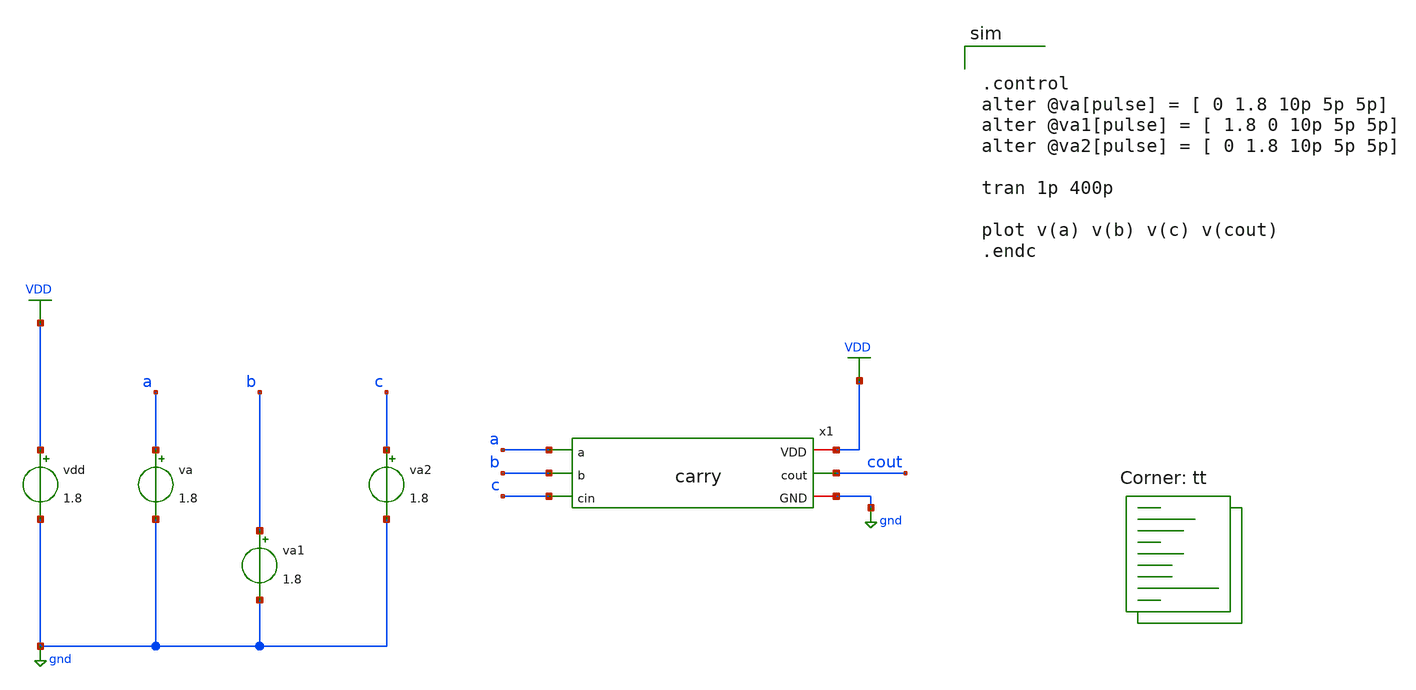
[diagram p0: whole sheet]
** sch_path: assignments/assignment7/carry_tb.sch
**.subckt carry_tb
x1 VDD a b c cout gnd carry
vdd VDD gnd 1.8
va a gnd 1.8
va1 b gnd 1.8
va2 c gnd 1.8
**** begin user architecture code


.control
alter @va[pulse] = [ 0 1.8 10p 5p 5p]
alter @va1[pulse] = [ 1.8 0 10p 5p 5p]
alter @va2[pulse] = [ 0 1.8 10p 5p 5p]

tran 1p 400p

plot v(a) v(b) v(c) v(cout)
.endc


.lib $::SKYWATER_MODELS/sky130.lib.spice tt
**** end user architecture code
**.ends

* expanding   symbol:  carry.sym # of pins=6
** sym_path: assignments/assignment7/carry.sym
** sch_path: assignments/assignment7/carry.sch
.subckt carry VDD a b cin cout GND
*.opin cout
*.ipin a
*.iopin VDD
*.iopin GND
*.ipin b
*.ipin cin
XM1 cout cin net3 GND sky130_fd_pr__nfet_01v8 L=0.15 W=0.84 nf=1 ad='int((nf+1)/2) * W/nf * 0.29' as='int((nf+2)/2) * W/nf * 0.29'
+ pd='2*int((nf+1)/2) * (W/nf + 0.29)' ps='2*int((nf+2)/2) * (W/nf + 0.29)' nrd='0.29 / W' nrs='0.29 / W'
+ sa=0 sb=0 sd=0 mult=1 m=1
XM2 net1 b VDD VDD sky130_fd_pr__pfet_01v8 L=0.15 W=1.68 nf=1 ad='int((nf+1)/2) * W/nf * 0.29' as='int((nf+2)/2) * W/nf * 0.29'
+ pd='2*int((nf+1)/2) * (W/nf + 0.29)' ps='2*int((nf+2)/2) * (W/nf + 0.29)' nrd='0.29 / W' nrs='0.29 / W'
+ sa=0 sb=0 sd=0 mult=1 m=1
XM3 net3 a GND GND sky130_fd_pr__nfet_01v8 L=0.15 W=0.84 nf=1 ad='int((nf+1)/2) * W/nf * 0.29' as='int((nf+2)/2) * W/nf * 0.29'
+ pd='2*int((nf+1)/2) * (W/nf + 0.29)' ps='2*int((nf+2)/2) * (W/nf + 0.29)' nrd='0.29 / W' nrs='0.29 / W'
+ sa=0 sb=0 sd=0 mult=1 m=1
XM4 cout cin net1 VDD sky130_fd_pr__pfet_01v8 L=0.15 W=1.68 nf=1 ad='int((nf+1)/2) * W/nf * 0.29' as='int((nf+2)/2) * W/nf * 0.29'
+ pd='2*int((nf+1)/2) * (W/nf + 0.29)' ps='2*int((nf+2)/2) * (W/nf + 0.29)' nrd='0.29 / W' nrs='0.29 / W'
+ sa=0 sb=0 sd=0 mult=1 m=1
XM5 net1 a VDD VDD sky130_fd_pr__pfet_01v8 L=0.15 W=1.68 nf=1 ad='int((nf+1)/2) * W/nf * 0.29' as='int((nf+2)/2) * W/nf * 0.29'
+ pd='2*int((nf+1)/2) * (W/nf + 0.29)' ps='2*int((nf+2)/2) * (W/nf + 0.29)' nrd='0.29 / W' nrs='0.29 / W'
+ sa=0 sb=0 sd=0 mult=1 m=1
XM6 net2 a VDD VDD sky130_fd_pr__pfet_01v8 L=0.15 W=1.68 nf=1 ad='int((nf+1)/2) * W/nf * 0.29' as='int((nf+2)/2) * W/nf * 0.29'
+ pd='2*int((nf+1)/2) * (W/nf + 0.29)' ps='2*int((nf+2)/2) * (W/nf + 0.29)' nrd='0.29 / W' nrs='0.29 / W'
+ sa=0 sb=0 sd=0 mult=1 m=1
XM7 cout b net2 VDD sky130_fd_pr__pfet_01v8 L=0.15 W=1.68 nf=1 ad='int((nf+1)/2) * W/nf * 0.29' as='int((nf+2)/2) * W/nf * 0.29'
+ pd='2*int((nf+1)/2) * (W/nf + 0.29)' ps='2*int((nf+2)/2) * (W/nf + 0.29)' nrd='0.29 / W' nrs='0.29 / W'
+ sa=0 sb=0 sd=0 mult=1 m=1
XM8 net3 b GND GND sky130_fd_pr__nfet_01v8 L=0.15 W=0.84 nf=1 ad='int((nf+1)/2) * W/nf * 0.29' as='int((nf+2)/2) * W/nf * 0.29'
+ pd='2*int((nf+1)/2) * (W/nf + 0.29)' ps='2*int((nf+2)/2) * (W/nf + 0.29)' nrd='0.29 / W' nrs='0.29 / W'
+ sa=0 sb=0 sd=0 mult=1 m=1
XM9 cout a net4 GND sky130_fd_pr__nfet_01v8 L=0.15 W=0.84 nf=1 ad='int((nf+1)/2) * W/nf * 0.29' as='int((nf+2)/2) * W/nf * 0.29'
+ pd='2*int((nf+1)/2) * (W/nf + 0.29)' ps='2*int((nf+2)/2) * (W/nf + 0.29)' nrd='0.29 / W' nrs='0.29 / W'
+ sa=0 sb=0 sd=0 mult=1 m=1
XM10 net4 b GND GND sky130_fd_pr__nfet_01v8 L=0.15 W=0.84 nf=1 ad='int((nf+1)/2) * W/nf * 0.29' as='int((nf+2)/2) * W/nf * 0.29'
+ pd='2*int((nf+1)/2) * (W/nf + 0.29)' ps='2*int((nf+2)/2) * (W/nf + 0.29)' nrd='0.29 / W' nrs='0.29 / W'
+ sa=0 sb=0 sd=0 mult=1 m=1
.ends

.GLOBAL gnd
.GLOBAL VDD
.end
